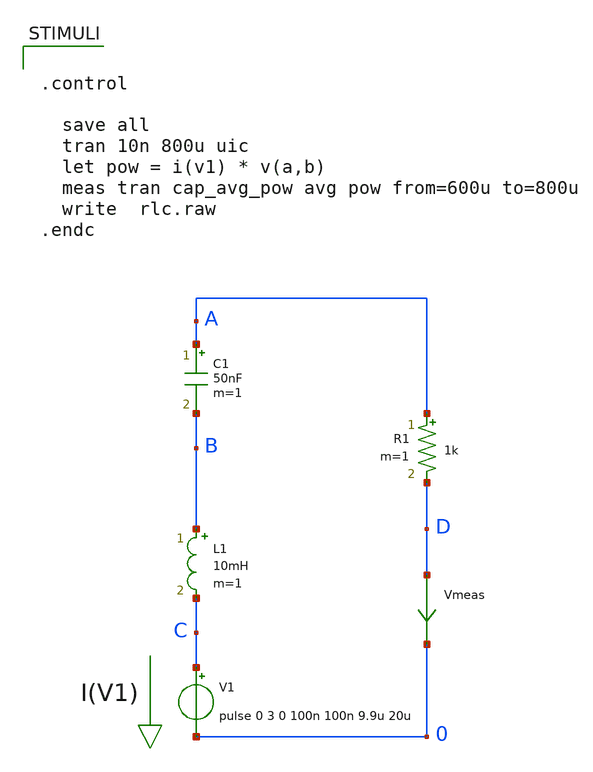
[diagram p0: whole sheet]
** sch_path: xschem_libs_newsym/examples/rlc/schematic/rlc.sch
* Copyright (C) 1998-2024 Stefan Frederik Schippers
* This program is free software; you can redistribute it and/or modify
* it under the terms of the GNU General Public License as published by
* the Free Software Foundation; either version 2 of the License, or
* (at your option) any later version.
* This program is distributed in the hope that it will be useful,
* but WITHOUT ANY WARRANTY; without even the implied warranty of
* MERCHANTABILITY or FITNESS FOR A PARTICULAR PURPOSE.  See the
* GNU General Public License for more details.
* You should have received a copy of the GNU General Public License
* along with this program; if not, write to the Free Software
**.subckt rlc
C1 A B 50nF m=1
R1 A D 1k m=1
L1 B C 10mH m=1
V1 C 0 pulse 0 3 0 100n 100n 9.9u 20u
Vmeas D 0 0
.save i(vmeas)
**** begin user architecture code


.control

  save all
  tran 10n 800u uic
  let pow = i(v1) * v(a,b)
  meas tran cap_avg_pow avg pow from=600u to=800u
  write  rlc.raw
.endc


**** end user architecture code
**.ends
.end
